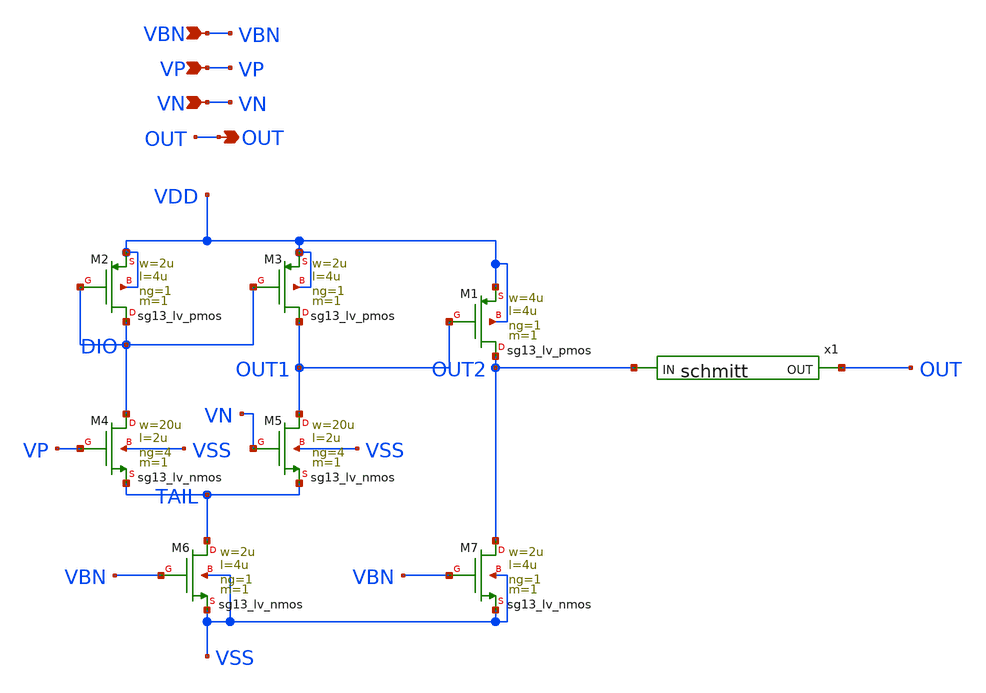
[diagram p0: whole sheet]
** sch_path: design/blocks/comparator/schematic/comp_sup.sch
**.subckt comp_sup OUT VN VP VBN
*.opin OUT
*.ipin VN
*.ipin VP
*.ipin VBN
XM2 DIO DIO VDD VDD sg13_lv_pmos w=2u l=4u ng=1 m=1 mm_ok=1
XM3 OUT1 DIO VDD VDD sg13_lv_pmos w=2u l=4u ng=1 m=1 mm_ok=1
XM4 DIO VP TAIL VSS sg13_lv_nmos w=20u l=2u ng=4 m=1 mm_ok=1
XM5 OUT1 VN TAIL VSS sg13_lv_nmos w=20u l=2u ng=4 m=1 mm_ok=1
XM6 TAIL VBN VSS VSS sg13_lv_nmos w=2u l=4u ng=1 m=1 mm_ok=1
XM1 OUT2 OUT1 VDD VDD sg13_lv_pmos w=4u l=4u ng=1 m=1 mm_ok=1
XM7 OUT2 VBN VSS VSS sg13_lv_nmos w=2u l=4u ng=1 m=1 mm_ok=1
x1 OUT2 OUT VDD VSS schmitt
**.ends

* expanding   symbol:  schmitt.sym # of pins=2
** sym_path: design/blocks/schmitt/schematic/schmitt.sym
** sch_path: design/blocks/schmitt/schematic/schmitt.sch
.subckt schmitt IN OUT VDD VSS
*.opin OUT
*.ipin IN
XM4 P_MID IN VDD VDD sg13_lv_pmos w=1.04u l=0.13u ng=1 m=1 mm_ok=1
XM6 OUT IN N_MID VSS sg13_lv_nmos w=0.76u l=0.13u ng=1 m=1 mm_ok=1
XM5 OUT IN P_MID VDD sg13_lv_pmos w=1.04u l=0.13u ng=1 m=1 mm_ok=1
XM7 N_MID IN VSS VSS sg13_lv_nmos w=0.76u l=0.13u ng=1 m=1 mm_ok=1
XM8 VSS OUT P_MID VDD sg13_lv_pmos w=0.42u l=0.13u ng=1 m=1 mm_ok=1
XM9 VDD OUT N_MID VSS sg13_lv_nmos w=0.42u l=0.13u ng=1 m=1 mm_ok=1
.ends

.end
